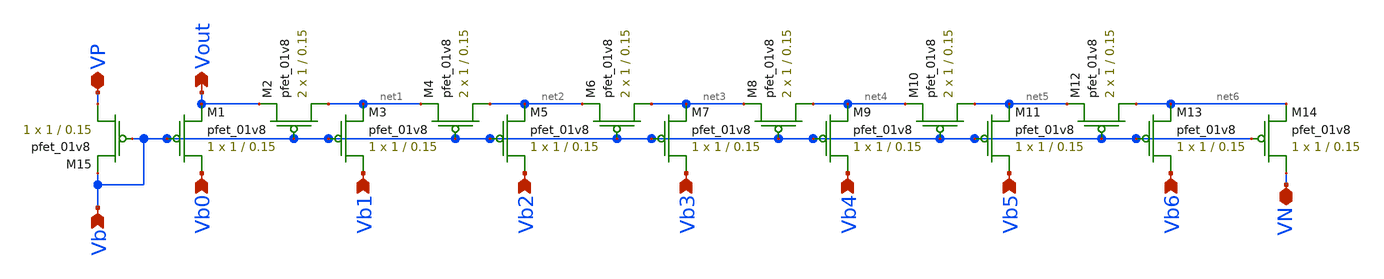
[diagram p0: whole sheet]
** sch_path: dac/schematics/misc/dac_pmos_donotuse.sch
**.subckt dac_pmos_donotuse VN VP Vb1 Vb Vout Vb2 Vb3 Vb4 Vb5 Vb6 Vb0
*.iopin VN
*.iopin VP
*.ipin Vb1
*.ipin Vb
*.opin Vout
*.ipin Vb2
*.ipin Vb3
*.ipin Vb4
*.ipin Vb5
*.ipin Vb6
*.ipin Vb0
XM1 Vb0 Vb Vout VDD sky130_fd_pr__pfet_01v8 L=0.15 W=1 nf=1 ad='int((nf+1)/2) * W/nf * 0.29' as='int((nf+2)/2) * W/nf * 0.29'
+ pd='2*int((nf+1)/2) * (W/nf + 0.29)' ps='2*int((nf+2)/2) * (W/nf + 0.29)' nrd='0.29 / W' nrs='0.29 / W'
+ sa=0 sb=0 sd=0 mult=1 m=1
XM2 net1 Vb Vout VDD sky130_fd_pr__pfet_01v8 L=0.15 W=1 nf=1 ad='int((nf+1)/2) * W/nf * 0.29' as='int((nf+2)/2) * W/nf * 0.29'
+ pd='2*int((nf+1)/2) * (W/nf + 0.29)' ps='2*int((nf+2)/2) * (W/nf + 0.29)' nrd='0.29 / W' nrs='0.29 / W'
+ sa=0 sb=0 sd=0 mult=2 m=2
XM3 Vb1 Vb net1 VDD sky130_fd_pr__pfet_01v8 L=0.15 W=1 nf=1 ad='int((nf+1)/2) * W/nf * 0.29' as='int((nf+2)/2) * W/nf * 0.29'
+ pd='2*int((nf+1)/2) * (W/nf + 0.29)' ps='2*int((nf+2)/2) * (W/nf + 0.29)' nrd='0.29 / W' nrs='0.29 / W'
+ sa=0 sb=0 sd=0 mult=1 m=1
XM4 net2 Vb net1 VDD sky130_fd_pr__pfet_01v8 L=0.15 W=1 nf=1 ad='int((nf+1)/2) * W/nf * 0.29' as='int((nf+2)/2) * W/nf * 0.29'
+ pd='2*int((nf+1)/2) * (W/nf + 0.29)' ps='2*int((nf+2)/2) * (W/nf + 0.29)' nrd='0.29 / W' nrs='0.29 / W'
+ sa=0 sb=0 sd=0 mult=2 m=2
XM5 Vb2 Vb net2 VDD sky130_fd_pr__pfet_01v8 L=0.15 W=1 nf=1 ad='int((nf+1)/2) * W/nf * 0.29' as='int((nf+2)/2) * W/nf * 0.29'
+ pd='2*int((nf+1)/2) * (W/nf + 0.29)' ps='2*int((nf+2)/2) * (W/nf + 0.29)' nrd='0.29 / W' nrs='0.29 / W'
+ sa=0 sb=0 sd=0 mult=1 m=1
XM6 net3 Vb net2 VDD sky130_fd_pr__pfet_01v8 L=0.15 W=1 nf=1 ad='int((nf+1)/2) * W/nf * 0.29' as='int((nf+2)/2) * W/nf * 0.29'
+ pd='2*int((nf+1)/2) * (W/nf + 0.29)' ps='2*int((nf+2)/2) * (W/nf + 0.29)' nrd='0.29 / W' nrs='0.29 / W'
+ sa=0 sb=0 sd=0 mult=2 m=2
XM7 Vb3 Vb net3 VDD sky130_fd_pr__pfet_01v8 L=0.15 W=1 nf=1 ad='int((nf+1)/2) * W/nf * 0.29' as='int((nf+2)/2) * W/nf * 0.29'
+ pd='2*int((nf+1)/2) * (W/nf + 0.29)' ps='2*int((nf+2)/2) * (W/nf + 0.29)' nrd='0.29 / W' nrs='0.29 / W'
+ sa=0 sb=0 sd=0 mult=1 m=1
XM8 net4 Vb net3 VDD sky130_fd_pr__pfet_01v8 L=0.15 W=1 nf=1 ad='int((nf+1)/2) * W/nf * 0.29' as='int((nf+2)/2) * W/nf * 0.29'
+ pd='2*int((nf+1)/2) * (W/nf + 0.29)' ps='2*int((nf+2)/2) * (W/nf + 0.29)' nrd='0.29 / W' nrs='0.29 / W'
+ sa=0 sb=0 sd=0 mult=2 m=2
XM9 Vb4 Vb net4 VDD sky130_fd_pr__pfet_01v8 L=0.15 W=1 nf=1 ad='int((nf+1)/2) * W/nf * 0.29' as='int((nf+2)/2) * W/nf * 0.29'
+ pd='2*int((nf+1)/2) * (W/nf + 0.29)' ps='2*int((nf+2)/2) * (W/nf + 0.29)' nrd='0.29 / W' nrs='0.29 / W'
+ sa=0 sb=0 sd=0 mult=1 m=1
XM10 net5 Vb net4 VDD sky130_fd_pr__pfet_01v8 L=0.15 W=1 nf=1 ad='int((nf+1)/2) * W/nf * 0.29' as='int((nf+2)/2) * W/nf * 0.29'
+ pd='2*int((nf+1)/2) * (W/nf + 0.29)' ps='2*int((nf+2)/2) * (W/nf + 0.29)' nrd='0.29 / W' nrs='0.29 / W'
+ sa=0 sb=0 sd=0 mult=2 m=2
XM11 Vb5 Vb net5 VDD sky130_fd_pr__pfet_01v8 L=0.15 W=1 nf=1 ad='int((nf+1)/2) * W/nf * 0.29' as='int((nf+2)/2) * W/nf * 0.29'
+ pd='2*int((nf+1)/2) * (W/nf + 0.29)' ps='2*int((nf+2)/2) * (W/nf + 0.29)' nrd='0.29 / W' nrs='0.29 / W'
+ sa=0 sb=0 sd=0 mult=1 m=1
XM12 net6 Vb net5 VDD sky130_fd_pr__pfet_01v8 L=0.15 W=1 nf=1 ad='int((nf+1)/2) * W/nf * 0.29' as='int((nf+2)/2) * W/nf * 0.29'
+ pd='2*int((nf+1)/2) * (W/nf + 0.29)' ps='2*int((nf+2)/2) * (W/nf + 0.29)' nrd='0.29 / W' nrs='0.29 / W'
+ sa=0 sb=0 sd=0 mult=2 m=2
XM13 Vb6 Vb net6 VDD sky130_fd_pr__pfet_01v8 L=0.15 W=1 nf=1 ad='int((nf+1)/2) * W/nf * 0.29' as='int((nf+2)/2) * W/nf * 0.29'
+ pd='2*int((nf+1)/2) * (W/nf + 0.29)' ps='2*int((nf+2)/2) * (W/nf + 0.29)' nrd='0.29 / W' nrs='0.29 / W'
+ sa=0 sb=0 sd=0 mult=1 m=1
XM14 VN Vb net6 VDD sky130_fd_pr__pfet_01v8 L=0.15 W=1 nf=1 ad='int((nf+1)/2) * W/nf * 0.29' as='int((nf+2)/2) * W/nf * 0.29'
+ pd='2*int((nf+1)/2) * (W/nf + 0.29)' ps='2*int((nf+2)/2) * (W/nf + 0.29)' nrd='0.29 / W' nrs='0.29 / W'
+ sa=0 sb=0 sd=0 mult=1 m=1
XM15 VP Vb Vb VDD sky130_fd_pr__pfet_01v8 L=0.15 W=1 nf=1 ad='int((nf+1)/2) * W/nf * 0.29' as='int((nf+2)/2) * W/nf * 0.29'
+ pd='2*int((nf+1)/2) * (W/nf + 0.29)' ps='2*int((nf+2)/2) * (W/nf + 0.29)' nrd='0.29 / W' nrs='0.29 / W'
+ sa=0 sb=0 sd=0 mult=1 m=1
**.ends
.end
